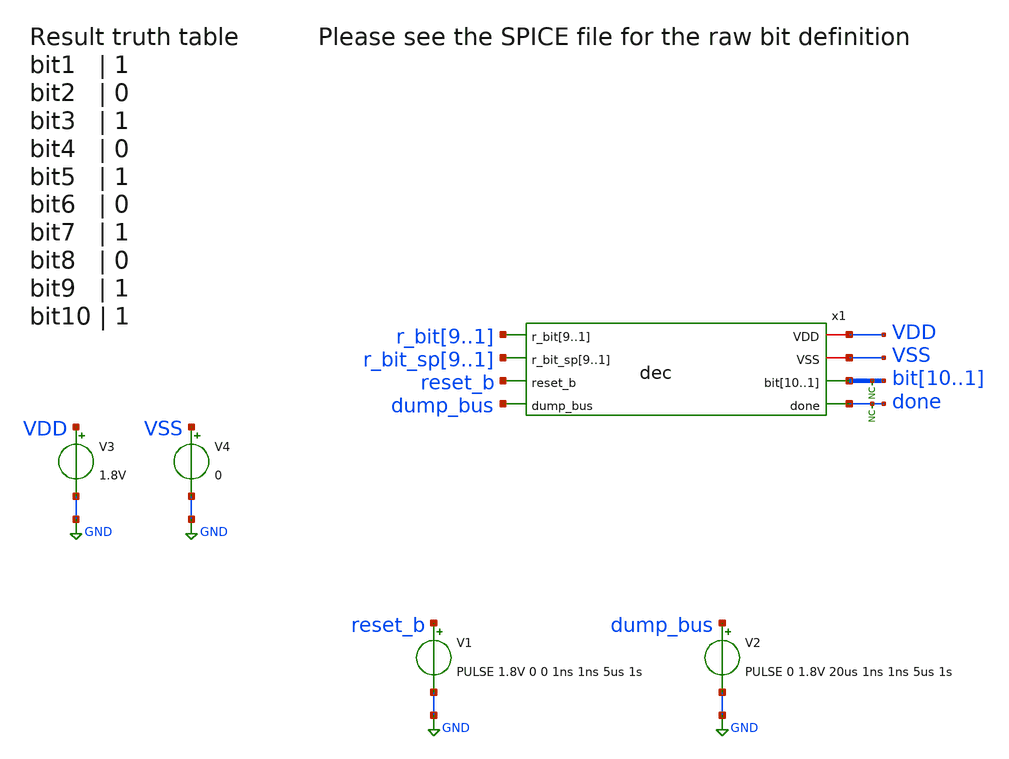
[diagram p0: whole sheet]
** sch_path: xschem/tests/dec/dec_test.sch
**.subckt dec_test
V3 VDD GND 1.8V
V4 VSS GND 0
x1 VDD r_bit9 r_bit8 r_bit7 r_bit6 r_bit5 r_bit4 r_bit3 r_bit2 r_bit1 VSS r_bit_sp9 r_bit_sp8
+ r_bit_sp7 r_bit_sp6 r_bit_sp5 r_bit_sp4 r_bit_sp3 r_bit_sp2 r_bit_sp1 bit10 bit9 bit8 bit7 bit6 bit5 bit4
+ bit3 bit2 bit1 reset_b done dump_bus dec
V1 reset_b GND PULSE 1.8V 0 0 1ns 1ns 5us 1s
V2 dump_bus GND PULSE 0 1.8V 20us 1ns 1ns 5us 1s
* noconn done
* noconn bit[10..1]
**** begin user architecture code
 .lib $::SKYWATER_MODELS/sky130.lib.spice tt
.include $::SKYWATER_STDCELLS/sky130_fd_sc_hd.spice


.options acct list
.temp 25
*vvcc VDD 0 dc 1.8

* * Create the input raw bits
* v_ref1 r_bit1 0 dc 1.8
* v_ref2 r_bit2 0 dc 0
* v_ref3 r_bit3 0 dc 1.8
* v_ref4 r_bit4 0 dc 0
* v_ref5 r_bit5 0 dc 1.8
* v_ref6 r_bit6 0 dc 0
* v_ref7 r_bit7 0 dc 1.8
* v_ref8 r_bit8 0 dc 0
* v_ref9 r_bit9 0 dc 1.8
*
* * Create the input raw bits for the split caps
* v_ref_sp1 r_bit_sp1 0 dc 1.8
* v_ref_sp2 r_bit_sp2 0 dc 0
* v_ref_sp3 r_bit_sp3 0 dc 1.8
* v_ref_sp4 r_bit_sp4 0 dc 0
* v_ref_sp5 r_bit_sp5 0 dc 1.8
* v_ref_sp6 r_bit_sp6 0 dc 0
* v_ref_sp7 r_bit_sp7 0 dc 1.8
* v_ref_sp8 r_bit_sp8 0 dc 0
* v_ref_sp9 r_bit_sp9 0 dc 1.8



* Create the input raw bits
v_ref1 r_bit1 0 dc 1.8
v_ref2 r_bit2 0 dc 1.8
v_ref3 r_bit3 0 dc 1.8
v_ref4 r_bit4 0 dc 1.8
v_ref5 r_bit5 0 dc 1.8
v_ref6 r_bit6 0 dc 1.8
v_ref7 r_bit7 0 dc 1.8
v_ref8 r_bit8 0 dc 1.8
v_ref9 r_bit9 0 dc 1.8

* Create the input raw bits for the split caps
v_ref_sp1 r_bit_sp1 0 dc 1.8
v_ref_sp2 r_bit_sp2 0 dc 1.8
v_ref_sp3 r_bit_sp3 0 dc 1.8
v_ref_sp4 r_bit_sp4 0 dc 1.8
v_ref_sp5 r_bit_sp5 0 dc 1.8
v_ref_sp6 r_bit_sp6 0 dc 1.8
v_ref_sp7 r_bit_sp7 0 dc 1.8
v_ref_sp8 r_bit_sp8 0 dc 1.8
v_ref_sp9 r_bit_sp9 0 dc 1.8


*vvss VSS 0 0
.control
tran 0.1u 50u
plot reset_b dump_bus+2 done+4 bit10+6 bit9+8 bit8+10
plot bit10 bit9+2 bit8+4 bit7+6 bit6+8 bit5+10 bit4+12 bit3+14 bit2+16 bit1+18
write pulse_generator_test.raw
.endc


**** end user architecture code
**.ends

* expanding   symbol:  src/dec/dec.sym # of pins=8
** sym_path: xschem/src/dec/dec.sym
** sch_path: xschem/src/dec/dec.sch
.subckt dec VDD r_bit9 r_bit8 r_bit7 r_bit6 r_bit5 r_bit4 r_bit3 r_bit2 r_bit1 VSS r_bit_sp9
+ r_bit_sp8 r_bit_sp7 r_bit_sp6 r_bit_sp5 r_bit_sp4 r_bit_sp3 r_bit_sp2 r_bit_sp1 bit10 bit9 bit8 bit7 bit6
+ bit5 bit4 bit3 bit2 bit1 reset_b done dump_bus
*.ipin r_bit9,r_bit8,r_bit7,r_bit6,r_bit5,r_bit4,r_bit3,r_bit2,r_bit1
*.iopin VDD
*.opin bit10,bit9,bit8,bit7,bit6,bit5,bit4,bit3,bit2,bit1
*.iopin VSS
*.ipin r_bit_sp9,r_bit_sp8,r_bit_sp7,r_bit_sp6,r_bit_sp5,r_bit_sp4,r_bit_sp3,r_bit_sp2,r_bit_sp1
*.ipin reset_b
*.ipin dump_bus
*.opin done
x62 r_bit_sp1 r_bit1 net1 VSS VSS VDD VDD net16 net2 sky130_fd_sc_hd__fa_1
x64 r_bit_sp2 r_bit2 net4 VSS VSS VDD VDD net1 net3 sky130_fd_sc_hd__fa_1
x67 dump_bus net2 reset_b VSS VSS VDD VDD bit2 sky130_fd_sc_hd__dfrtp_1
x68 dump_bus net3 reset_b VSS VSS VDD VDD bit3 sky130_fd_sc_hd__dfrtp_1
x65 r_bit_sp3 r_bit3 net5 VSS VSS VDD VDD net4 net6 sky130_fd_sc_hd__fa_1
x69 r_bit_sp4 r_bit4 net8 VSS VSS VDD VDD net5 net7 sky130_fd_sc_hd__fa_1
x70 dump_bus net6 reset_b VSS VSS VDD VDD bit4 sky130_fd_sc_hd__dfrtp_1
x71 dump_bus net7 reset_b VSS VSS VDD VDD bit5 sky130_fd_sc_hd__dfrtp_1
x72 r_bit_sp5 r_bit5 net9 VSS VSS VDD VDD net8 net10 sky130_fd_sc_hd__fa_1
x73 r_bit_sp6 r_bit6 net12 VSS VSS VDD VDD net9 net11 sky130_fd_sc_hd__fa_1
x74 dump_bus net10 reset_b VSS VSS VDD VDD bit6 sky130_fd_sc_hd__dfrtp_1
x75 dump_bus net11 reset_b VSS VSS VDD VDD bit7 sky130_fd_sc_hd__dfrtp_1
x76 r_bit_sp7 r_bit7 net13 VSS VSS VDD VDD net12 net14 sky130_fd_sc_hd__fa_1
x77 r_bit_sp8 r_bit8 r_bit_sp9 VSS VSS VDD VDD net13 net15 sky130_fd_sc_hd__fa_1
x78 dump_bus net14 reset_b VSS VSS VDD VDD bit8 sky130_fd_sc_hd__dfrtp_1
x79 dump_bus net15 reset_b VSS VSS VDD VDD bit9 sky130_fd_sc_hd__dfrtp_1
x80 dump_bus net16 reset_b VSS VSS VDD VDD bit1 sky130_fd_sc_hd__dfrtp_1
x81 dump_bus r_bit9 reset_b VSS VSS VDD VDD bit10 sky130_fd_sc_hd__dfrtp_1
x82 dump_bus VSS VSS VDD VDD done sky130_fd_sc_hd__inv_1
* noconn done
.ends

.GLOBAL GND
.end
